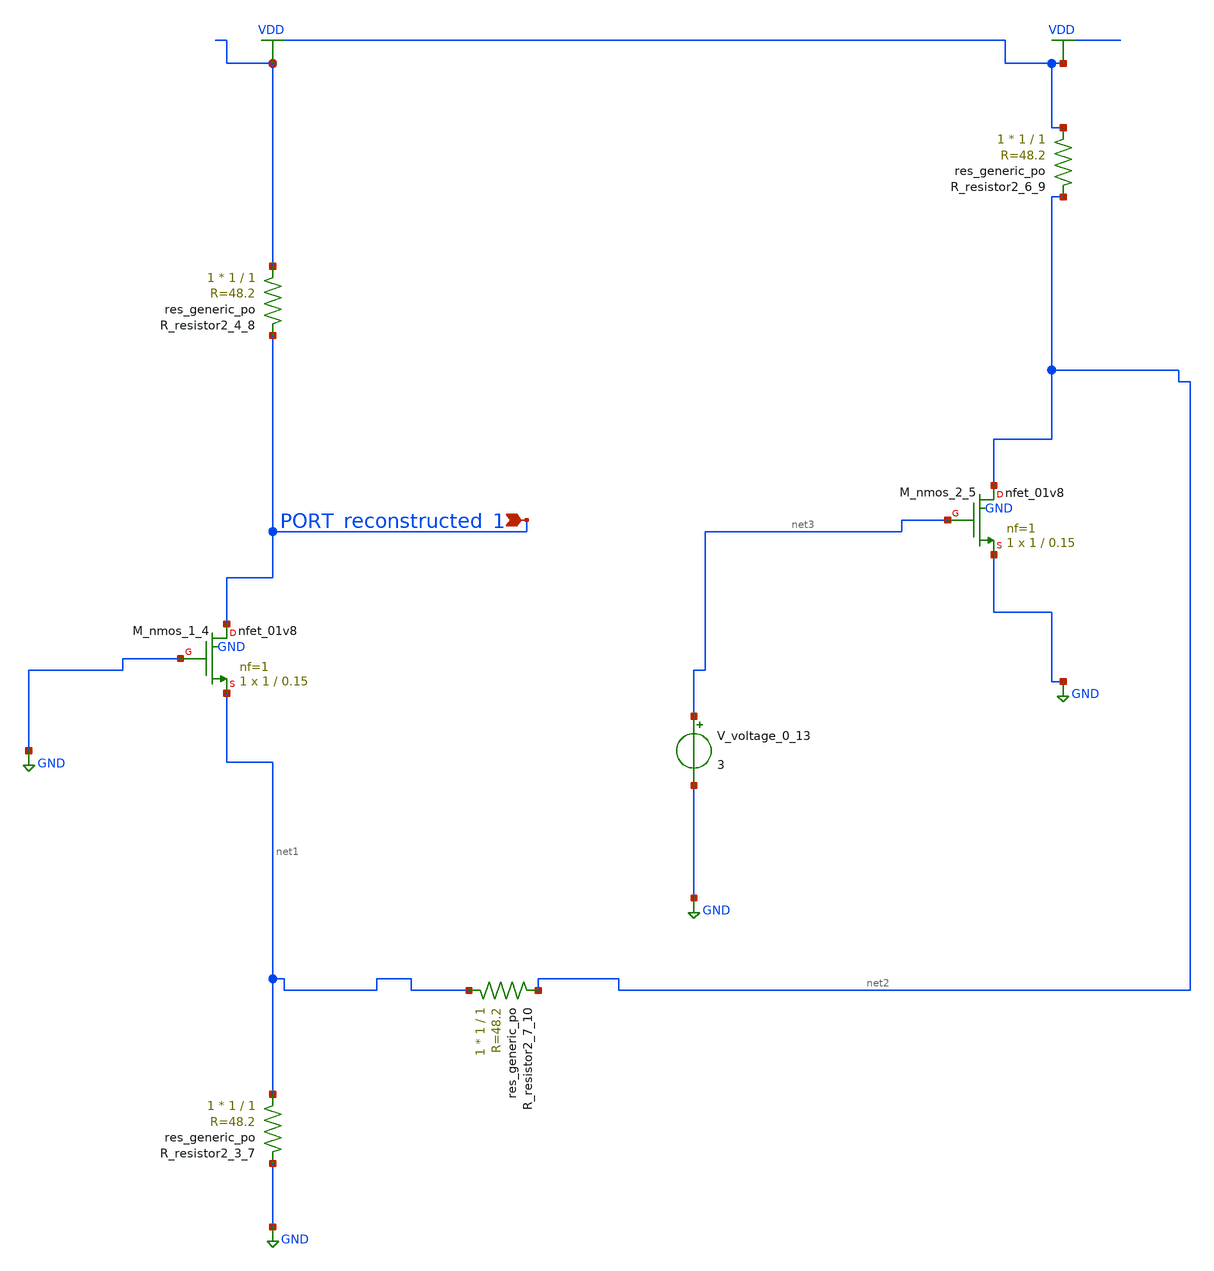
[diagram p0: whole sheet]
** sch_path: schematics/AMSNet/597.sch
**.subckt 597 PORT_reconstructed_1
*.ipin PORT_reconstructed_1
XM_nmos_1_4 PORT_reconstructed_1 GND net1 GND sky130_fd_pr__nfet_01v8 L=0.15 W=1 nf=1 ad='int((1 + 1)/2) * 1 / 1 * 0.29'
+ as='int((1 + 2)/2) * 1 / 1 * 0.29' pd='2*int((1 + 1)/2) * (1 / 1 + 0.29)' ps='2*int((1 + 2)/2) * (1 / 1 + 0.29)'
+ nrd='0.29 / 1 ' nrs='0.29 / 1 ' sa=0 sb=0 sd=0 mult=1 m=1
XM_nmos_2_5 net2 net3 GND GND sky130_fd_pr__nfet_01v8 L=0.15 W=1 nf=1 ad='int((1 + 1)/2) * 1 / 1 * 0.29'
+ as='int((1 + 2)/2) * 1 / 1 * 0.29' pd='2*int((1 + 1)/2) * (1 / 1 + 0.29)' ps='2*int((1 + 2)/2) * (1 / 1 + 0.29)'
+ nrd='0.29 / 1 ' nrs='0.29 / 1 ' sa=0 sb=0 sd=0 mult=1 m=1
XR_resistor2_3_7 net1 GND sky130_fd_pr__res_generic_po W=1 L=1 m=1
XR_resistor2_4_8 VDD PORT_reconstructed_1 sky130_fd_pr__res_generic_po W=1 L=1 m=1
XR_resistor2_6_9 VDD net2 sky130_fd_pr__res_generic_po W=1 L=1 m=1
XR_resistor2_7_10 net1 net2 sky130_fd_pr__res_generic_po W=1 L=1 m=1
V_voltage_0_13 net3 GND 3
**.ends
.GLOBAL GND
.GLOBAL VDD
.end
